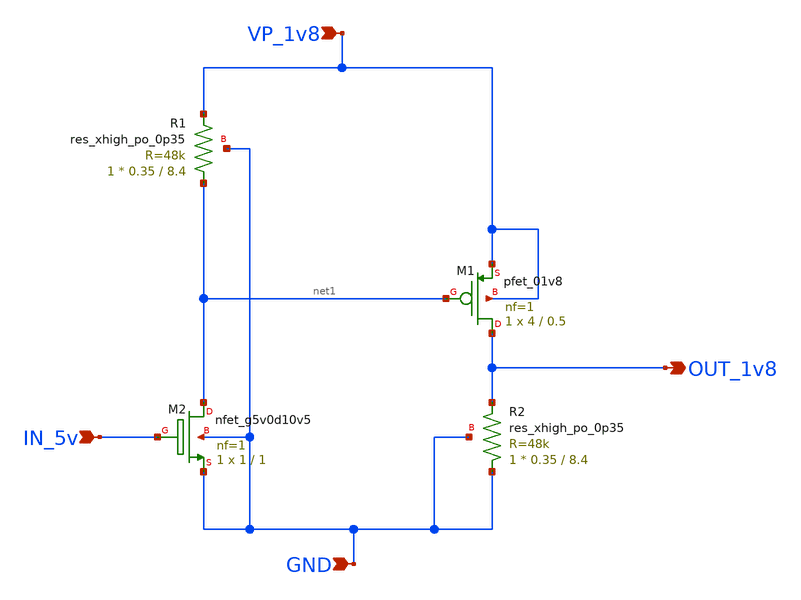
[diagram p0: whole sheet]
** sch_path: ADC/16bit_C2C/MagicAndSpice/EE431_FinalProj/Shift_5v_to_1v8.sch
**.subckt Shift_5v_to_1v8 IN_5v VP_1v8 GND OUT_1v8
*.ipin IN_5v
*.ipin VP_1v8
*.ipin GND
*.opin OUT_1v8
XM1 OUT_1v8 net1 VP_1v8 VP_1v8 sky130_fd_pr__pfet_01v8 L=0.5 W=4 nf=1 ad='int((nf+1)/2) * W/nf * 0.29'
+ as='int((nf+2)/2) * W/nf * 0.29' pd='2*int((nf+1)/2) * (W/nf + 0.29)' ps='2*int((nf+2)/2) * (W/nf + 0.29)'
+ nrd='0.29 / W' nrs='0.29 / W' sa=0 sb=0 sd=0 mult=1 m=1
XM2 net1 IN_5v GND GND sky130_fd_pr__nfet_g5v0d10v5 L=1 W=1 nf=1 ad='int((nf+1)/2) * W/nf * 0.29' as='int((nf+2)/2) * W/nf * 0.29'
+ pd='2*int((nf+1)/2) * (W/nf + 0.29)' ps='2*int((nf+2)/2) * (W/nf + 0.29)' nrd='0.29 / W' nrs='0.29 / W'
+ sa=0 sb=0 sd=0 mult=1 m=1
XR1 net1 VP_1v8 GND sky130_fd_pr__res_xhigh_po_0p35 L=8.4 mult=1 m=1
XR2 GND OUT_1v8 GND sky130_fd_pr__res_xhigh_po_0p35 L=8.4 mult=1 m=1
**.ends
.end
